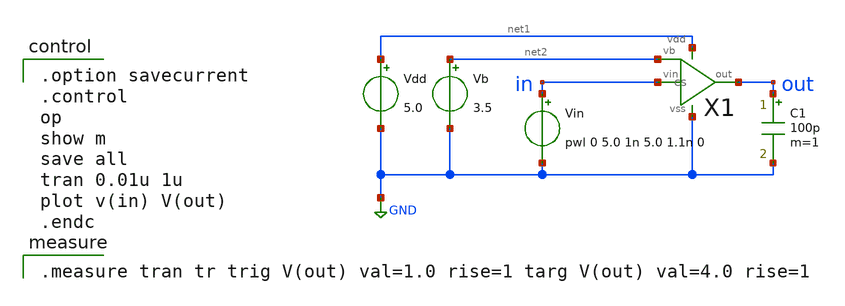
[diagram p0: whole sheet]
** sch_path: member_project/OPAMP/ShuntaroOhno/xschem/cs_tran.sch
**.subckt cs_tran
Vdd net1 GND 5.0
Vb net2 GND 3.5
C1 out GND 100p m=1
Vin in GND pwl 0 5.0 1n 5.0 1.1n 0
X1 in net2 out net1 GND cs
**** begin user architecture code

.option savecurrent
.control
op
show m
save all
tran 0.01u 1u
plot v(in) V(out)
.endc


.measure tran tr trig V(out) val=1.0 rise=1 targ V(out) val=4.0 rise=1

 .include $::LIB/../ip62_models
**** end user architecture code
**.ends

* expanding   symbol:  cs.sym # of pins=5
** sym_path: cs.sym
** sch_path: cs.sch
.subckt cs vin vb out vdd vss
*.ipin vb
*.ipin vin
*.opin out
*.iopin vss
*.iopin vdd
XM6 out vb vdd vdd PMOS w=540u l=3u as=0 ad=0 ps=0 pd=0 nrd=0 nrs=0 m=1
XM7 out vin vss vss NMOS w=270u l=3u as=0 ad=0 ps=0 pd=0 nrd=0 nrs=0 m=1
.ends

.GLOBAL GND
.end
